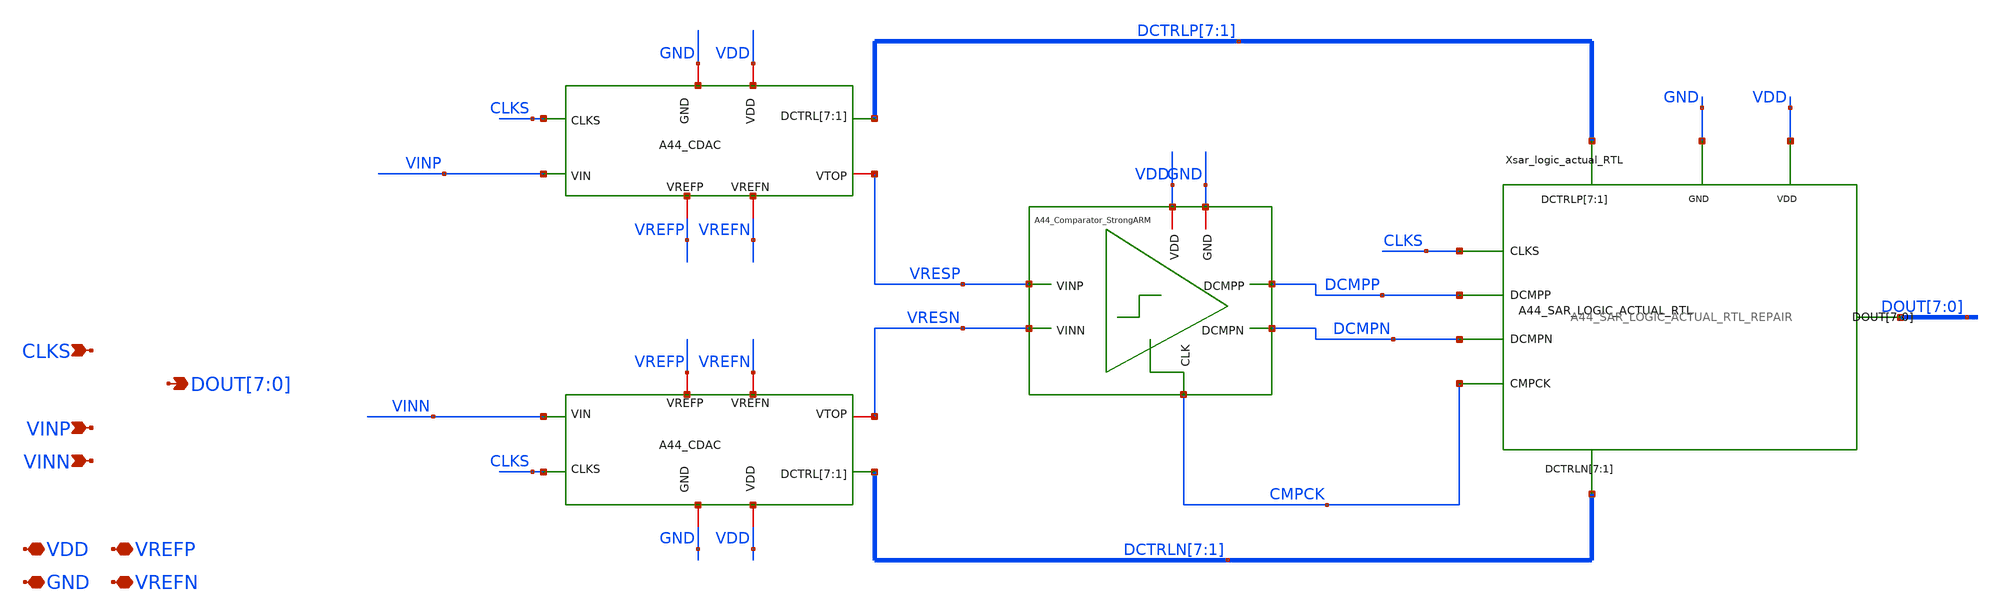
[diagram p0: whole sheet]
** sch_path: verification/a44_r2/01_CURRENT_CIRCUIT_FILES/xschem/SAR_ADC_TOP_FIXED.sch
**.subckt SAR_ADC_TOP_FIXED VDD GND VREFP VREFN CLKS VINP VINN
*+ DOUT[7],DOUT[6],DOUT[5],DOUT[4],DOUT[3],DOUT[2],DOUT[1],DOUT[0]
*.iopin VDD
*.iopin GND
*.iopin VREFP
*.iopin VREFN
*.ipin CLKS
*.ipin VINP
*.ipin VINN
*.opin DOUT[7],DOUT[6],DOUT[5],DOUT[4],DOUT[3],DOUT[2],DOUT[1],DOUT[0]
x1 CMPCK DCMPP VRESP DCMPN VRESN VDD GND Comparator_StrongARM
x2 VINP CLKS VRESP DCTRLP[7] DCTRLP[6] DCTRLP[5] DCTRLP[4] DCTRLP[3] DCTRLP[2] DCTRLP[1] VREFP VDD
+ GND VREFN CDAC
x3 VINN CLKS VRESN DCTRLN[7] DCTRLN[6] DCTRLN[5] DCTRLN[4] DCTRLN[3] DCTRLN[2] DCTRLN[1] VREFP VDD
+ GND VREFN CDAC
Xsar_logic_actual_RTL CLKS DCMPP DCMPN CMPCK DCTRLP_7 DCTRLP_6 DCTRLP_5 DCTRLP_4 DCTRLP_3 DCTRLP_2
+ DCTRLP_1 DCTRLN_7 DCTRLN_6 DCTRLN_5 DCTRLN_4 DCTRLN_3 DCTRLN_2 DCTRLN_1 DOUT_7 DOUT_6 DOUT_5 DOUT_4 DOUT_3
+ DOUT_2 DOUT_1 DOUT_0 VDD GND SAR_LOGIC_ACTUAL_RTL
**.ends
.end
